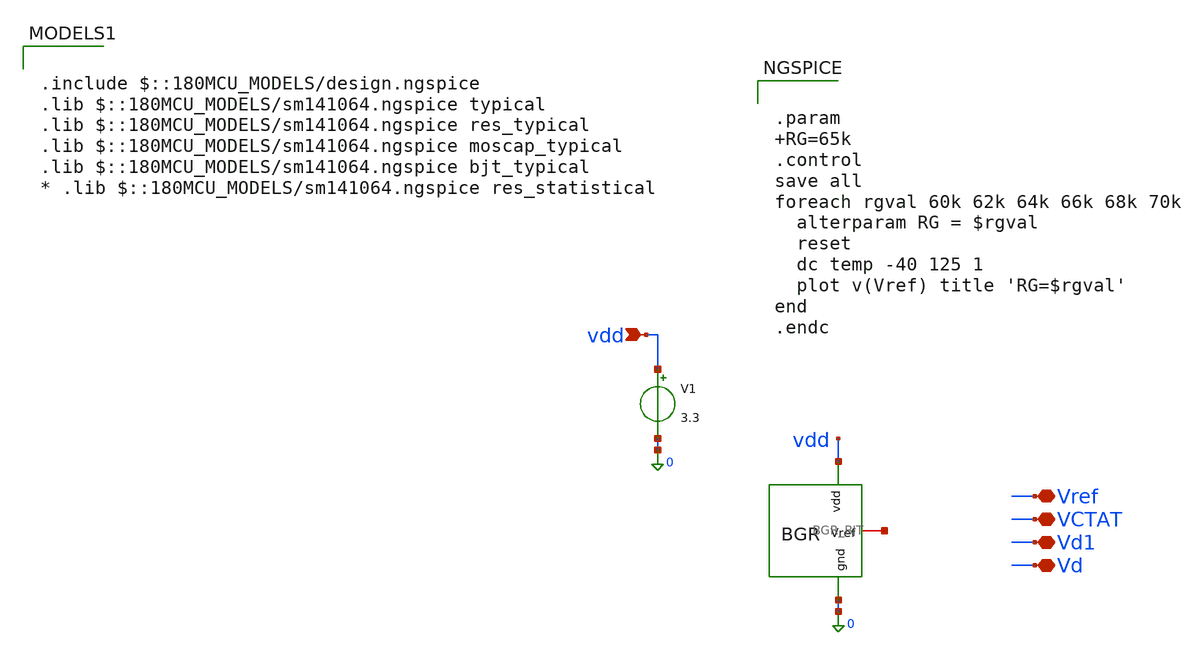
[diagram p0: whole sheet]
** sch_path: xschem/bias_generator/BGR_BJT_dc.sch
**.subckt BGR_BJT_dc vdd Vref VCTAT Vd1 Vd
*.ipin vdd
*.iopin Vref
*.iopin VCTAT
*.iopin Vd1
*.iopin Vd
V1 vdd 0 3.3
x1 vdd net1 0 BGR_BJT
**** begin user architecture code


.param RG=65k
.control
save all
foreach rgval 60k 62k 64k 66k 68k 70k
  alterparam RG = $rgval
  reset
  dc temp -40 125 1
  plot v(Vref) title 'RG=$rgval'
end
.endc



.include $::180MCU_MODELS/design.ngspice
.lib $::180MCU_MODELS/sm141064.ngspice typical
.lib $::180MCU_MODELS/sm141064.ngspice res_typical
.lib $::180MCU_MODELS/sm141064.ngspice moscap_typical
.lib $::180MCU_MODELS/sm141064.ngspice bjt_typical
* .lib $::180MCU_MODELS/sm141064.ngspice res_statistical

**** end user architecture code
**.ends

* expanding   symbol:  GF180/xschem/Chipathon/BGR/BGR_BJT.sym # of pins=3
** sym_path: xschem/bias_generator/BGR_BJT.sym
** sch_path: xschem/bias_generator/BGR_BJT.sch
.subckt BGR_BJT vdd Vref gnd
*.ipin gnd
*.iopin Vref
*.ipin vdd
XM2 net1 net2 vdd vdd pfet_03v3 L=4u W=10u nf=1 ad='int((nf+1)/2) * W/nf * 0.18u' as='int((nf+2)/2) * W/nf * 0.18u'
+ pd='2*int((nf+1)/2) * (W/nf + 0.18u)' ps='2*int((nf+2)/2) * (W/nf + 0.18u)' nrd='0.18u / W' nrs='0.18u / W'
+ sa=0 sb=0 sd=0 m=1
XM3 net2 net2 vdd vdd pfet_03v3 L=4u W=10u nf=1 ad='int((nf+1)/2) * W/nf * 0.18u' as='int((nf+2)/2) * W/nf * 0.18u'
+ pd='2*int((nf+1)/2) * (W/nf + 0.18u)' ps='2*int((nf+2)/2) * (W/nf + 0.18u)' nrd='0.18u / W' nrs='0.18u / W'
+ sa=0 sb=0 sd=0 m=1
XM4 Vref net2 vdd vdd pfet_03v3 L=4u W=10u nf=1 ad='int((nf+1)/2) * W/nf * 0.18u' as='int((nf+2)/2) * W/nf * 0.18u'
+ pd='2*int((nf+1)/2) * (W/nf + 0.18u)' ps='2*int((nf+2)/2) * (W/nf + 0.18u)' nrd='0.18u / W' nrs='0.18u / W'
+ sa=0 sb=0 sd=0 m=1
XM13 net1 net1 net5 gnd nfet_03v3 L=2u W=10u nf=1 ad='int((nf+1)/2) * W/nf * 0.18u' as='int((nf+2)/2) * W/nf * 0.18u'
+ pd='2*int((nf+1)/2) * (W/nf + 0.18u)' ps='2*int((nf+2)/2) * (W/nf + 0.18u)' nrd='0.18u / W' nrs='0.18u / W'
+ sa=0 sb=0 sd=0 m=1
XM14 net2 net1 net4 gnd nfet_03v3 L=2u W=10u nf=1 ad='int((nf+1)/2) * W/nf * 0.18u' as='int((nf+2)/2) * W/nf * 0.18u'
+ pd='2*int((nf+1)/2) * (W/nf + 0.18u)' ps='2*int((nf+2)/2) * (W/nf + 0.18u)' nrd='0.18u / W' nrs='0.18u / W'
+ sa=0 sb=0 sd=0 m=1
R1 Vref net7 66k m=1
R2 net4 net3 5k m=1
XQ1 gnd gnd net3 pnp_05p00x05p00 m=4 par=4
XQ2 gnd gnd net5 pnp_05p00x05p00 m=1 par=1
XM1 net2 net6 gnd gnd nfet_03v3 L=2u W=10u nf=1 ad='int((nf+1)/2) * W/nf * 0.18u' as='int((nf+2)/2) * W/nf * 0.18u'
+ pd='2*int((nf+1)/2) * (W/nf + 0.18u)' ps='2*int((nf+2)/2) * (W/nf + 0.18u)' nrd='0.18u / W' nrs='0.18u / W'
+ sa=0 sb=0 sd=0 m=1
XM5 vdd vdd net6 gnd nfet_03v3 L=0.5u W=1u nf=1 ad='int((nf+1)/2) * W/nf * 0.18u' as='int((nf+2)/2) * W/nf * 0.18u'
+ pd='2*int((nf+1)/2) * (W/nf + 0.18u)' ps='2*int((nf+2)/2) * (W/nf + 0.18u)' nrd='0.18u / W' nrs='0.18u / W'
+ sa=0 sb=0 sd=0 m=1
XM6 net6 net1 gnd gnd nfet_03v3 L=1u W=20u nf=1 ad='int((nf+1)/2) * W/nf * 0.18u' as='int((nf+2)/2) * W/nf * 0.18u'
+ pd='2*int((nf+1)/2) * (W/nf + 0.18u)' ps='2*int((nf+2)/2) * (W/nf + 0.18u)' nrd='0.18u / W' nrs='0.18u / W'
+ sa=0 sb=0 sd=0 m=1
XQ3 gnd gnd net7 pnp_05p00x05p00 m=1 par=1
.ends

.end
